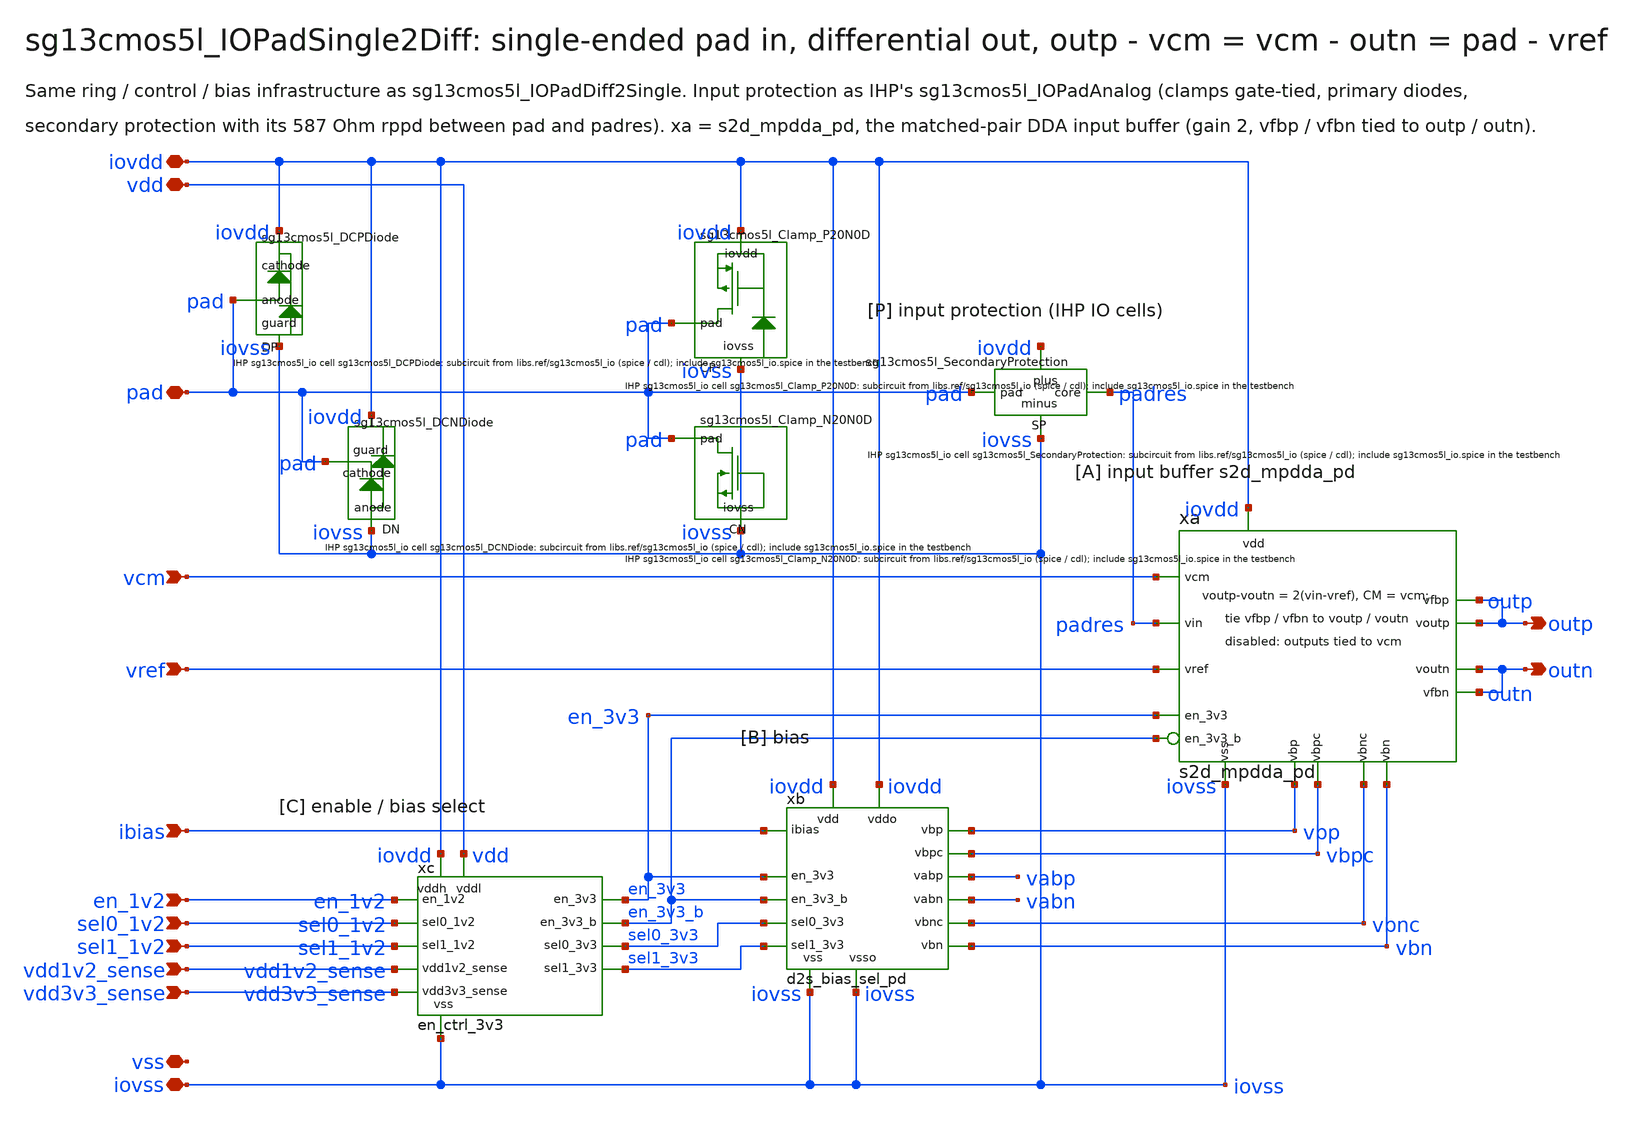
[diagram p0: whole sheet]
** sch_path: sudelbuecher/design_considerations/consolidation/bias_hierarchy_2026-10-27/before/macros/sg13cmos5l_IOPadSingle2Diff/schematic/xschem/sg13cmos5l_IOPadSingle2Diff.sch
**.subckt sg13cmos5l_IOPadSingle2Diff iovdd iovss vdd vss pad outp outn vcm vref ibias en_1v2
*+ sel0_1v2 sel1_1v2 vdd1v2_sense vdd3v3_sense
*.iopin iovdd
*.iopin iovss
*.iopin vdd
*.iopin vss
*.iopin pad
*.opin outp
*.opin outn
*.ipin vcm
*.ipin vref
*.ipin ibias
*.ipin en_1v2
*.ipin sel0_1v2
*.ipin sel1_1v2
*.ipin vdd1v2_sense
*.ipin vdd3v3_sense
xc iovdd vdd iovss en_1v2 sel0_1v2 sel1_1v2 vdd1v2_sense vdd3v3_sense en_3v3 sel0_3v3 sel1_3v3
+ en_3v3_b en_ctrl_3v3
xb iovdd iovss iovdd iovss ibias vbp vbn vbpc vbnc vabp vabn en_3v3 sel0_3v3 sel1_3v3 en_3v3_b
+ d2s_bias_sel_pd
xa iovdd iovss padres vref vcm outp outn outp outn vbp vbn vbpc vbnc en_3v3 en_3v3_b s2d_mpdda_pd
XCP iovdd iovss pad sg13cmos5l_Clamp_P20N0D
XCN iovss pad sg13cmos5l_Clamp_N20N0D
XDN iovss pad iovdd sg13cmos5l_DCNDiode
XDP pad iovdd iovss sg13cmos5l_DCPDiode
XSP padres iovss pad iovdd sg13cmos5l_SecondaryProtection
**.ends
.end
